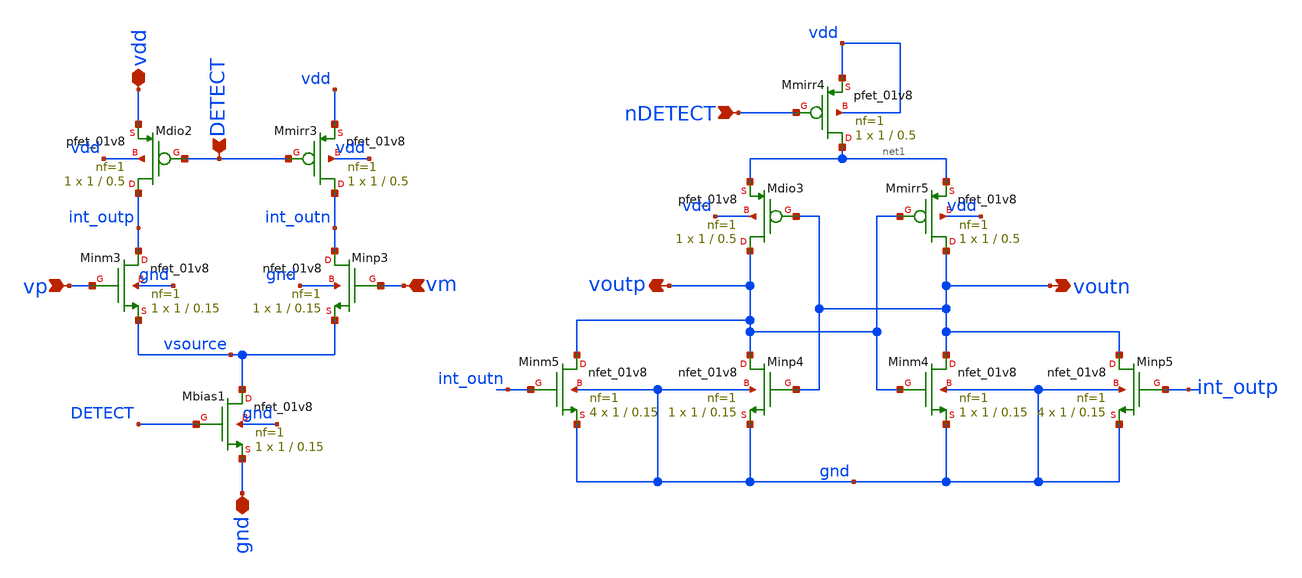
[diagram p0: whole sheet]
** sch_path: analog/xschem/col_amp_v2_std_vds/xschem/dyn_comp.sch
**.subckt dyn_comp vdd gnd vp vm nDETECT voutn voutp DETECT
*.iopin vdd
*.iopin gnd
*.ipin vp
*.ipin vm
*.ipin nDETECT
*.opin voutn
*.opin voutp
*.ipin DETECT
XMmirr3 int_outn DETECT vdd vdd sky130_fd_pr__pfet_01v8 L=0.5 W=1 nf=1 ad='int((1 + 1)/2) * 1 / 1 * 0.29'
+ as='int((1 + 2)/2) * 1 / 1 * 0.29' pd='2*int((1 + 1)/2) * (1 / 1 + 0.29)' ps='2*int((1 + 2)/2) * (1 / 1 + 0.29)'
+ nrd='0.29 / 1 ' nrs='0.29 / 1 ' sa=0 sb=0 sd=0 mult=1 m=1
XMdio2 int_outp DETECT vdd vdd sky130_fd_pr__pfet_01v8 L=0.5 W=1 nf=1 ad='int((1 + 1)/2) * 1 / 1 * 0.29'
+ as='int((1 + 2)/2) * 1 / 1 * 0.29' pd='2*int((1 + 1)/2) * (1 / 1 + 0.29)' ps='2*int((1 + 2)/2) * (1 / 1 + 0.29)'
+ nrd='0.29 / 1 ' nrs='0.29 / 1 ' sa=0 sb=0 sd=0 mult=1 m=1
XMinm3 int_outp vp vsource gnd sky130_fd_pr__nfet_01v8 L=0.15 W=1 nf=1 ad='int((1 + 1)/2) * 1 / 1 * 0.29'
+ as='int((1 + 2)/2) * 1 / 1 * 0.29' pd='2*int((1 + 1)/2) * (1 / 1 + 0.29)' ps='2*int((1 + 2)/2) * (1 / 1 + 0.29)'
+ nrd='0.29 / 1 ' nrs='0.29 / 1 ' sa=0 sb=0 sd=0 mult=1 m=1
XMinp3 int_outn vm vsource gnd sky130_fd_pr__nfet_01v8 L=0.15 W=1 nf=1 ad='int((1 + 1)/2) * 1 / 1 * 0.29'
+ as='int((1 + 2)/2) * 1 / 1 * 0.29' pd='2*int((1 + 1)/2) * (1 / 1 + 0.29)' ps='2*int((1 + 2)/2) * (1 / 1 + 0.29)'
+ nrd='0.29 / 1 ' nrs='0.29 / 1 ' sa=0 sb=0 sd=0 mult=1 m=1
XMbias1 vsource DETECT gnd gnd sky130_fd_pr__nfet_01v8 L=0.15 W=1 nf=1 ad='int((1 + 1)/2) * 1 / 1 * 0.29'
+ as='int((1 + 2)/2) * 1 / 1 * 0.29' pd='2*int((1 + 1)/2) * (1 / 1 + 0.29)' ps='2*int((1 + 2)/2) * (1 / 1 + 0.29)'
+ nrd='0.29 / 1 ' nrs='0.29 / 1 ' sa=0 sb=0 sd=0 mult=1 m=1
XMmirr4 net1 nDETECT vdd vdd sky130_fd_pr__pfet_01v8 L=0.5 W=1 nf=1 ad='int((1 + 1)/2) * 1 / 1 * 0.29'
+ as='int((1 + 2)/2) * 1 / 1 * 0.29' pd='2*int((1 + 1)/2) * (1 / 1 + 0.29)' ps='2*int((1 + 2)/2) * (1 / 1 + 0.29)'
+ nrd='0.29 / 1 ' nrs='0.29 / 1 ' sa=0 sb=0 sd=0 mult=1 m=1
XMmirr5 voutn voutp net1 vdd sky130_fd_pr__pfet_01v8 L=0.5 W=1 nf=1 ad='int((1 + 1)/2) * 1 / 1 * 0.29'
+ as='int((1 + 2)/2) * 1 / 1 * 0.29' pd='2*int((1 + 1)/2) * (1 / 1 + 0.29)' ps='2*int((1 + 2)/2) * (1 / 1 + 0.29)'
+ nrd='0.29 / 1 ' nrs='0.29 / 1 ' sa=0 sb=0 sd=0 mult=1 m=1
XMdio3 voutp voutn net1 vdd sky130_fd_pr__pfet_01v8 L=0.5 W=1 nf=1 ad='int((1 + 1)/2) * 1 / 1 * 0.29'
+ as='int((1 + 2)/2) * 1 / 1 * 0.29' pd='2*int((1 + 1)/2) * (1 / 1 + 0.29)' ps='2*int((1 + 2)/2) * (1 / 1 + 0.29)'
+ nrd='0.29 / 1 ' nrs='0.29 / 1 ' sa=0 sb=0 sd=0 mult=1 m=1
XMinp4 voutp voutn gnd gnd sky130_fd_pr__nfet_01v8 L=0.15 W=1 nf=1 ad='int((1 + 1)/2) * 1 / 1 * 0.29'
+ as='int((1 + 2)/2) * 1 / 1 * 0.29' pd='2*int((1 + 1)/2) * (1 / 1 + 0.29)' ps='2*int((1 + 2)/2) * (1 / 1 + 0.29)'
+ nrd='0.29 / 1 ' nrs='0.29 / 1 ' sa=0 sb=0 sd=0 mult=1 m=1
XMinm4 voutn voutp gnd gnd sky130_fd_pr__nfet_01v8 L=0.15 W=1 nf=1 ad='int((1 + 1)/2) * 1 / 1 * 0.29'
+ as='int((1 + 2)/2) * 1 / 1 * 0.29' pd='2*int((1 + 1)/2) * (1 / 1 + 0.29)' ps='2*int((1 + 2)/2) * (1 / 1 + 0.29)'
+ nrd='0.29 / 1 ' nrs='0.29 / 1 ' sa=0 sb=0 sd=0 mult=1 m=1
XMinm5 voutp int_outn gnd gnd sky130_fd_pr__nfet_01v8 L=0.15 W=1 nf=1 ad='int((1 + 1)/2) * 1 / 1 * 0.29'
+ as='int((1 + 2)/2) * 1 / 1 * 0.29' pd='2*int((1 + 1)/2) * (1 / 1 + 0.29)' ps='2*int((1 + 2)/2) * (1 / 1 + 0.29)'
+ nrd='0.29 / 1 ' nrs='0.29 / 1 ' sa=0 sb=0 sd=0 mult=4 m=4
XMinp5 voutn int_outp gnd gnd sky130_fd_pr__nfet_01v8 L=0.15 W=1 nf=1 ad='int((1 + 1)/2) * 1 / 1 * 0.29'
+ as='int((1 + 2)/2) * 1 / 1 * 0.29' pd='2*int((1 + 1)/2) * (1 / 1 + 0.29)' ps='2*int((1 + 2)/2) * (1 / 1 + 0.29)'
+ nrd='0.29 / 1 ' nrs='0.29 / 1 ' sa=0 sb=0 sd=0 mult=4 m=4
**.ends
.end
